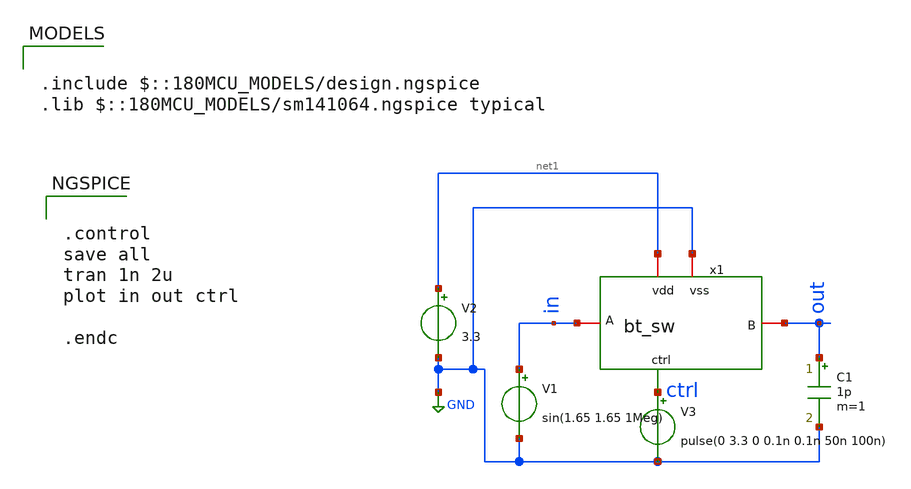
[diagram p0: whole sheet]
** sch_path: member_project/ice458/dynamic_comparator/xschem/bt_sw_tb.sch
**.subckt bt_sw_tb
V2 net1 GND 3.3
V3 ctrl GND pulse(0 3.3 0 0.1n 0.1n 50n 100n)
C1 out GND 1p m=1
x1 net1 in out GND ctrl bt_sw
V1 in GND sin(1.65 1.65 1Meg)
**** begin user architecture code

.include $::180MCU_MODELS/design.ngspice
.lib $::180MCU_MODELS/sm141064.ngspice typical



.control
save all
tran 1n 2u
plot in out ctrl

.endc


**** end user architecture code
**.ends

* expanding   symbol:  bt_sw.sym # of pins=5
** sym_path: member_project/ice458/dynamic_comparator/xschem/bt_sw.sym
** sch_path: member_project/ice458/dynamic_comparator/xschem/bt_sw.sch
.subckt bt_sw vdd A B vss ctrl
*.ipin ctrl
*.iopin A
*.iopin B
*.iopin vdd
*.iopin vss
XM1 A net5 B vss nfet_03v3 L=0.28u W=2.8u nf=1 ad='int((nf+1)/2) * W/nf * 0.18u' as='int((nf+2)/2) * W/nf * 0.18u'
+ pd='2*int((nf+1)/2) * (W/nf + 0.18u)' ps='2*int((nf+2)/2) * (W/nf + 0.18u)' nrd='0.18u / W' nrs='0.18u / W'
+ sa=0 sb=0 sd=0 m=1
C2 net1 net2 900f m=1
XM8 net3 net5 net2 vss nfet_03v3 L=0.28u W=0.22u nf=1 ad='int((nf+1)/2) * W/nf * 0.18u' as='int((nf+2)/2) * W/nf * 0.18u'
+ pd='2*int((nf+1)/2) * (W/nf + 0.18u)' ps='2*int((nf+2)/2) * (W/nf + 0.18u)' nrd='0.18u / W' nrs='0.18u / W'
+ sa=0 sb=0 sd=0 m=1
x3 vdd ctrl net4 vss inv
XM13 net1 net5 vdd vdd pfet_03v3 L=0.28u W=1u nf=1 ad='int((nf+1)/2) * W/nf * 0.18u' as='int((nf+2)/2) * W/nf * 0.18u'
+ pd='2*int((nf+1)/2) * (W/nf + 0.18u)' ps='2*int((nf+2)/2) * (W/nf + 0.18u)' nrd='0.18u / W' nrs='0.18u / W'
+ sa=0 sb=0 sd=0 m=1
XM3 net2 net4 vss vss nfet_03v3 L=0.28u W=0.42u nf=1 ad='int((nf+1)/2) * W/nf * 0.18u' as='int((nf+2)/2) * W/nf * 0.18u'
+ pd='2*int((nf+1)/2) * (W/nf + 0.18u)' ps='2*int((nf+2)/2) * (W/nf + 0.18u)' nrd='0.18u / W' nrs='0.18u / W'
+ sa=0 sb=0 sd=0 m=1
XM5 net3 ctrl net2 vss nfet_03v3 L=0.28u W=0.42u nf=1 ad='int((nf+1)/2) * W/nf * 0.18u' as='int((nf+2)/2) * W/nf * 0.18u'
+ pd='2*int((nf+1)/2) * (W/nf + 0.18u)' ps='2*int((nf+2)/2) * (W/nf + 0.18u)' nrd='0.18u / W' nrs='0.18u / W'
+ sa=0 sb=0 sd=0 m=1
XM9 A net5 net2 vss nfet_03v3 L=0.28u W=0.42u nf=1 ad='int((nf+1)/2) * W/nf * 0.18u' as='int((nf+2)/2) * W/nf * 0.18u'
+ pd='2*int((nf+1)/2) * (W/nf + 0.18u)' ps='2*int((nf+2)/2) * (W/nf + 0.18u)' nrd='0.18u / W' nrs='0.18u / W'
+ sa=0 sb=0 sd=0 m=1
XM10 net5 vdd net6 vss nfet_03v3 L=0.28u W=0.42u nf=1 ad='int((nf+1)/2) * W/nf * 0.18u' as='int((nf+2)/2) * W/nf * 0.18u'
+ pd='2*int((nf+1)/2) * (W/nf + 0.18u)' ps='2*int((nf+2)/2) * (W/nf + 0.18u)' nrd='0.18u / W' nrs='0.18u / W'
+ sa=0 sb=0 sd=0 m=1
XM11 net6 net4 vss vss nfet_03v3 L=0.28u W=0.42u nf=1 ad='int((nf+1)/2) * W/nf * 0.18u' as='int((nf+2)/2) * W/nf * 0.18u'
+ pd='2*int((nf+1)/2) * (W/nf + 0.18u)' ps='2*int((nf+2)/2) * (W/nf + 0.18u)' nrd='0.18u / W' nrs='0.18u / W'
+ sa=0 sb=0 sd=0 m=1
XM2 net3 net5 net7 vdd pfet_03v3 L=0.28u W=1u nf=1 ad='int((nf+1)/2) * W/nf * 0.18u' as='int((nf+2)/2) * W/nf * 0.18u'
+ pd='2*int((nf+1)/2) * (W/nf + 0.18u)' ps='2*int((nf+2)/2) * (W/nf + 0.18u)' nrd='0.18u / W' nrs='0.18u / W'
+ sa=0 sb=0 sd=0 m=1
XM4 net7 ctrl vdd vdd pfet_03v3 L=0.28u W=1u nf=1 ad='int((nf+1)/2) * W/nf * 0.18u' as='int((nf+2)/2) * W/nf * 0.18u'
+ pd='2*int((nf+1)/2) * (W/nf + 0.18u)' ps='2*int((nf+2)/2) * (W/nf + 0.18u)' nrd='0.18u / W' nrs='0.18u / W'
+ sa=0 sb=0 sd=0 m=1
XM6 net5 net3 net1 net1 pfet_03v3 L=0.28u W=1u nf=1 ad='int((nf+1)/2) * W/nf * 0.18u' as='int((nf+2)/2) * W/nf * 0.18u'
+ pd='2*int((nf+1)/2) * (W/nf + 0.18u)' ps='2*int((nf+2)/2) * (W/nf + 0.18u)' nrd='0.18u / W' nrs='0.18u / W'
+ sa=0 sb=0 sd=0 m=1
.ends


* expanding   symbol:  inv.sym # of pins=4
** sym_path: member_project/ice458/dynamic_comparator/xschem/inv.sym
** sch_path: member_project/ice458/dynamic_comparator/xschem/inv.sch
.subckt inv vdd a y vss
*.iopin vdd
*.iopin vss
*.ipin a
*.opin y
XM1 y a vss vss nfet_03v3 L=0.28u W=0.42u nf=1 ad='int((nf+1)/2) * W/nf * 0.18u' as='int((nf+2)/2) * W/nf * 0.18u'
+ pd='2*int((nf+1)/2) * (W/nf + 0.18u)' ps='2*int((nf+2)/2) * (W/nf + 0.18u)' nrd='0.18u / W' nrs='0.18u / W'
+ sa=0 sb=0 sd=0 m=1
XM2 y a vdd vdd pfet_03v3 L=0.28u W=1u nf=1 ad='int((nf+1)/2) * W/nf * 0.18u' as='int((nf+2)/2) * W/nf * 0.18u'
+ pd='2*int((nf+1)/2) * (W/nf + 0.18u)' ps='2*int((nf+2)/2) * (W/nf + 0.18u)' nrd='0.18u / W' nrs='0.18u / W'
+ sa=0 sb=0 sd=0 m=1
.ends

.GLOBAL GND
.end
